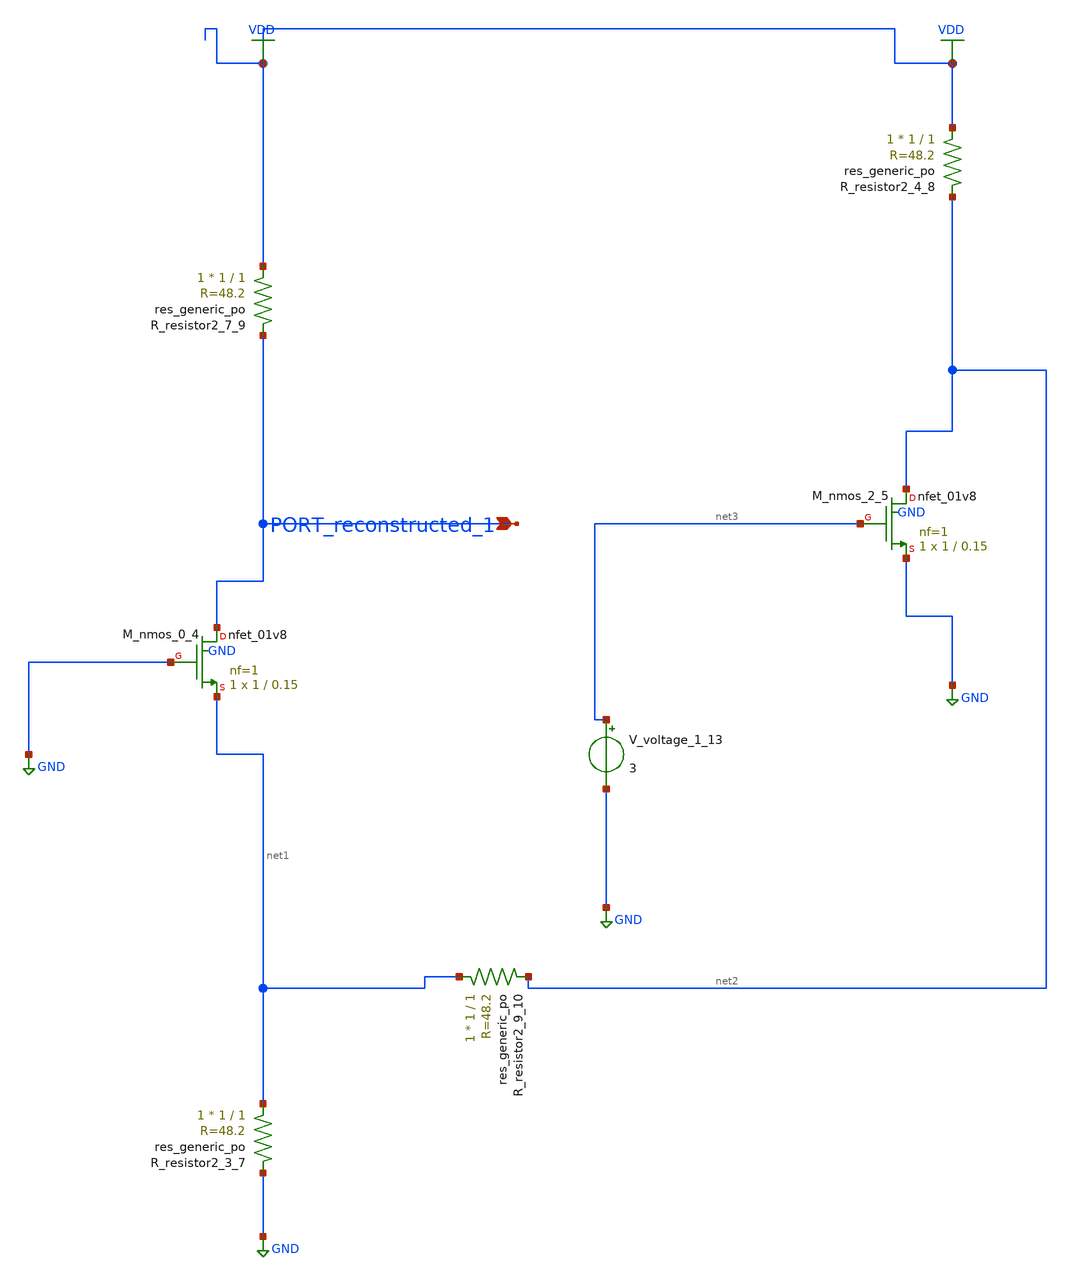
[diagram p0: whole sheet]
** sch_path: schematics/AMSNet/567.sch
**.subckt 567 PORT_reconstructed_1
*.ipin PORT_reconstructed_1
XM_nmos_0_4 PORT_reconstructed_1 GND net1 GND sky130_fd_pr__nfet_01v8 L=0.15 W=1 nf=1 ad='int((1 + 1)/2) * 1 / 1 * 0.29'
+ as='int((1 + 2)/2) * 1 / 1 * 0.29' pd='2*int((1 + 1)/2) * (1 / 1 + 0.29)' ps='2*int((1 + 2)/2) * (1 / 1 + 0.29)'
+ nrd='0.29 / 1 ' nrs='0.29 / 1 ' sa=0 sb=0 sd=0 mult=1 m=1
XM_nmos_2_5 net2 net3 GND GND sky130_fd_pr__nfet_01v8 L=0.15 W=1 nf=1 ad='int((1 + 1)/2) * 1 / 1 * 0.29'
+ as='int((1 + 2)/2) * 1 / 1 * 0.29' pd='2*int((1 + 1)/2) * (1 / 1 + 0.29)' ps='2*int((1 + 2)/2) * (1 / 1 + 0.29)'
+ nrd='0.29 / 1 ' nrs='0.29 / 1 ' sa=0 sb=0 sd=0 mult=1 m=1
XR_resistor2_3_7 net1 GND sky130_fd_pr__res_generic_po W=1 L=1 m=1
XR_resistor2_4_8 VDD net2 sky130_fd_pr__res_generic_po W=1 L=1 m=1
XR_resistor2_7_9 VDD PORT_reconstructed_1 sky130_fd_pr__res_generic_po W=1 L=1 m=1
XR_resistor2_9_10 net1 net2 sky130_fd_pr__res_generic_po W=1 L=1 m=1
V_voltage_1_13 net3 GND 3
**.ends
.GLOBAL GND
.GLOBAL VDD
.end
